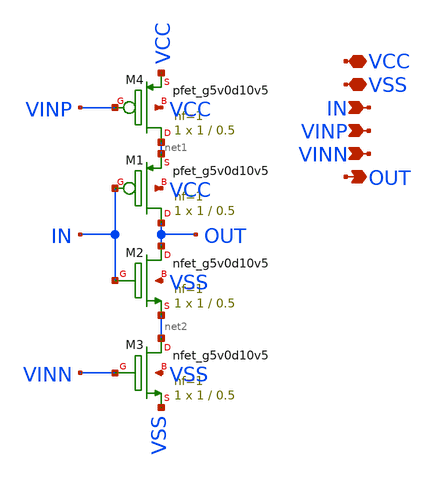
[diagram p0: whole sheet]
** sch_path: Comparator/schematic/Edge_pursuit_comparator/delay_cell.sch
**.subckt delay_cell VCC OUT VINP VINN VSS IN
*.iopin VCC
*.opin OUT
*.ipin VINP
*.ipin VINN
*.iopin VSS
*.ipin IN
XM1 OUT IN net1 VCC sky130_fd_pr__pfet_g5v0d10v5 L=0.5 W=1 nf=1 ad='int((nf+1)/2) * W/nf * 0.29' as='int((nf+2)/2) * W/nf * 0.29'
+ pd='2*int((nf+1)/2) * (W/nf + 0.29)' ps='2*int((nf+2)/2) * (W/nf + 0.29)' nrd='0.29 / W' nrs='0.29 / W'
+ sa=0 sb=0 sd=0 mult=1 m=1
XM2 OUT IN net2 VSS sky130_fd_pr__nfet_g5v0d10v5 L=0.5 W=1 nf=1 ad='int((nf+1)/2) * W/nf * 0.29' as='int((nf+2)/2) * W/nf * 0.29'
+ pd='2*int((nf+1)/2) * (W/nf + 0.29)' ps='2*int((nf+2)/2) * (W/nf + 0.29)' nrd='0.29 / W' nrs='0.29 / W'
+ sa=0 sb=0 sd=0 mult=1 m=1
XM3 net2 VINN VSS VSS sky130_fd_pr__nfet_g5v0d10v5 L=0.5 W=1 nf=1 ad='int((nf+1)/2) * W/nf * 0.29' as='int((nf+2)/2) * W/nf * 0.29'
+ pd='2*int((nf+1)/2) * (W/nf + 0.29)' ps='2*int((nf+2)/2) * (W/nf + 0.29)' nrd='0.29 / W' nrs='0.29 / W'
+ sa=0 sb=0 sd=0 mult=1 m=1
XM4 net1 VINP VCC VCC sky130_fd_pr__pfet_g5v0d10v5 L=0.5 W=1 nf=1 ad='int((nf+1)/2) * W/nf * 0.29' as='int((nf+2)/2) * W/nf * 0.29'
+ pd='2*int((nf+1)/2) * (W/nf + 0.29)' ps='2*int((nf+2)/2) * (W/nf + 0.29)' nrd='0.29 / W' nrs='0.29 / W'
+ sa=0 sb=0 sd=0 mult=1 m=1
**.ends
.end
